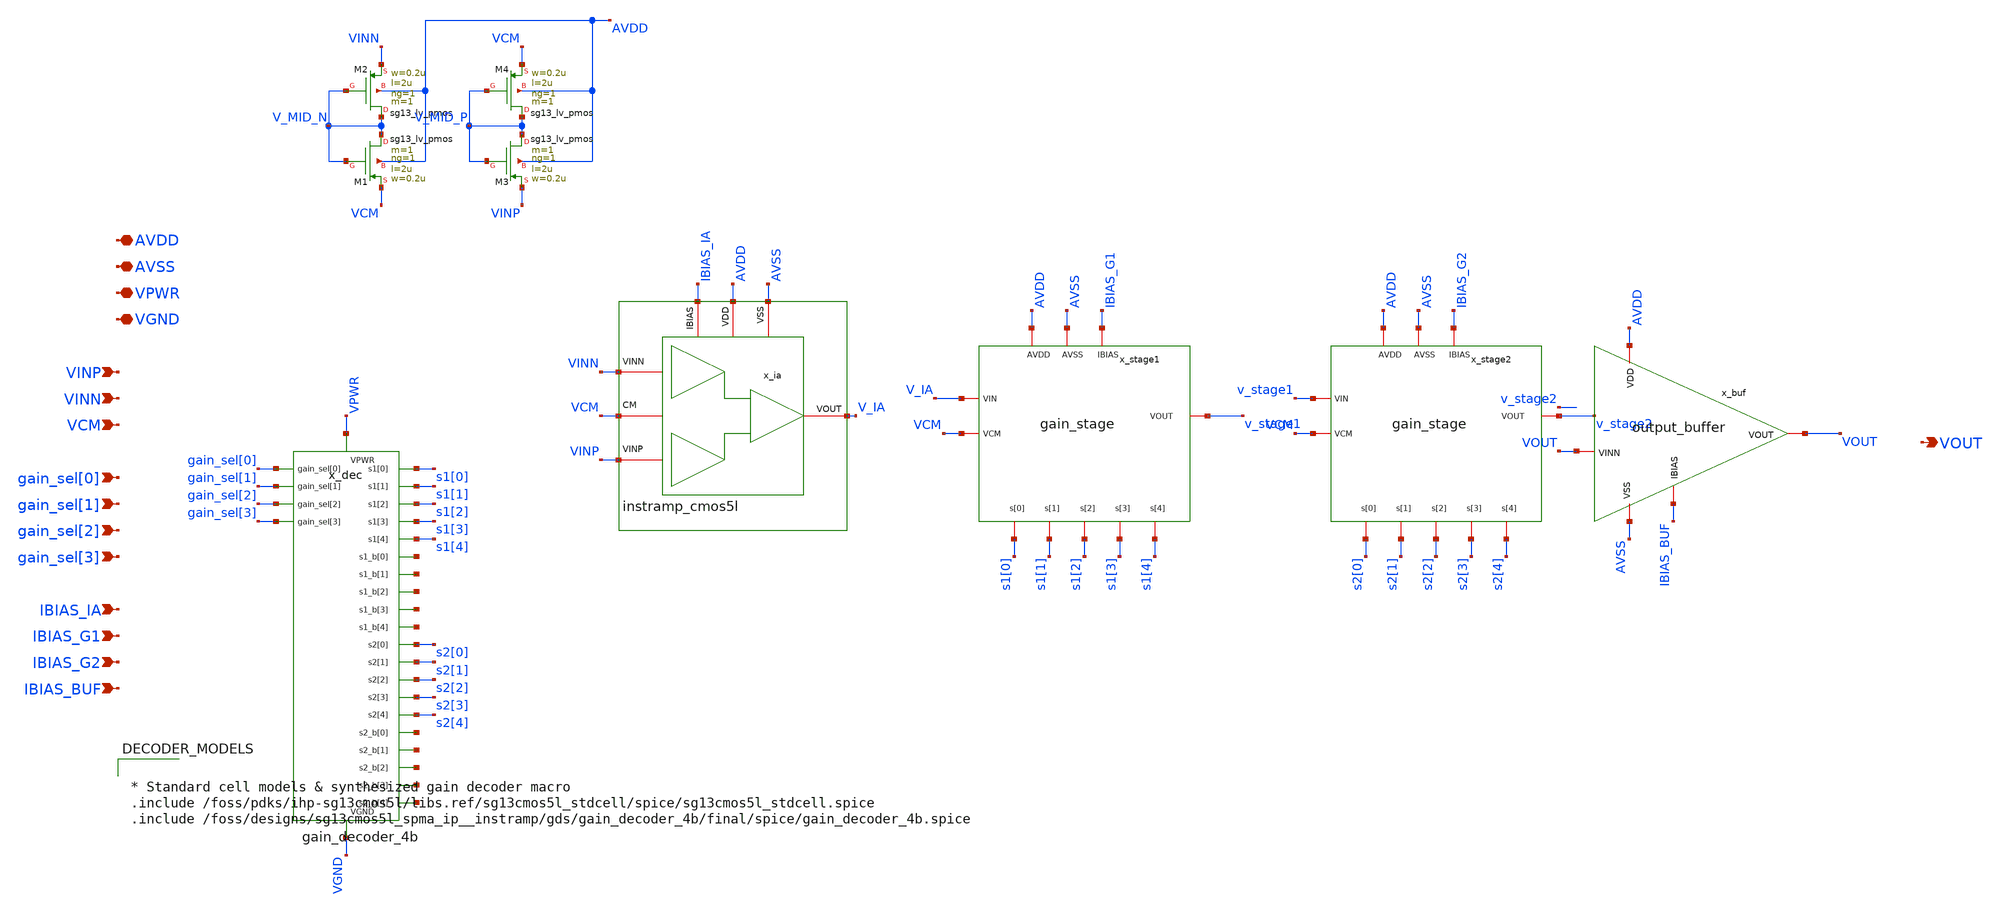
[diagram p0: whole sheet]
** sch_path: xschem/pgia_top/pgia_top.sch
**.subckt pgia_top AVDD AVSS VPWR VGND VINP VINN VCM gain_sel[0] gain_sel[1] gain_sel[2] gain_sel[3]
*+ IBIAS_IA IBIAS_G1 IBIAS_G2 IBIAS_BUF VOUT
*.iopin AVDD
*.iopin AVSS
*.iopin VPWR
*.iopin VGND
*.ipin VINP
*.ipin VINN
*.ipin VCM
*.ipin gain_sel[0]
*.ipin gain_sel[1]
*.ipin gain_sel[2]
*.ipin gain_sel[3]
*.ipin IBIAS_IA
*.ipin IBIAS_G1
*.ipin IBIAS_G2
*.ipin IBIAS_BUF
*.opin VOUT
x_dec VGND VPWR gain_sel[0] gain_sel[1] gain_sel[2] gain_sel[3] s1[0] s1[1] s1[2] s1[3] s1[4] net1
+ net2 net3 net4 net5 s2[0] s2[1] s2[2] s2[3] s2[4] net6 net7 net8 net9 net10 gain_decoder_4b
x_ia AVSS AVDD IBIAS_IA VINN V_IA VINP VCM instramp_cmos5l
x_stage1 AVDD AVSS IBIAS_G1 V_IA VCM v_stage1 s1[0] s1[1] s1[2] s1[3] s1[4] gain_stage
x_stage2 AVDD AVSS IBIAS_G2 v_stage1 VCM v_stage2 s2[0] s2[1] s2[2] s2[3] s2[4] gain_stage
x_buf AVDD AVSS IBIAS_BUF VOUT VOUT output_buffer
XM1 V_MID_N V_MID_N VCM AVDD sg13_lv_pmos w=0.2u l=2u ng=1 m=1 mm_ok=1
XM2 V_MID_N V_MID_N VINN AVDD sg13_lv_pmos w=0.2u l=2u ng=1 m=1 mm_ok=1
XM3 V_MID_P V_MID_P VINP AVDD sg13_lv_pmos w=0.2u l=2u ng=1 m=1 mm_ok=1
XM4 V_MID_P V_MID_P VCM AVDD sg13_lv_pmos w=0.2u l=2u ng=1 m=1 mm_ok=1
**** begin user architecture code


* Standard cell models & synthesized gain decoder macro
.include /foss/pdks/ihp-sg13cmos5l/libs.ref/sg13cmos5l_stdcell/spice/sg13cmos5l_stdcell.spice
.include /foss/designs/sg13cmos5l_spma_ip__instramp/gds/gain_decoder_4b/final/spice/gain_decoder_4b.spice


**** end user architecture code
**.ends
.end
